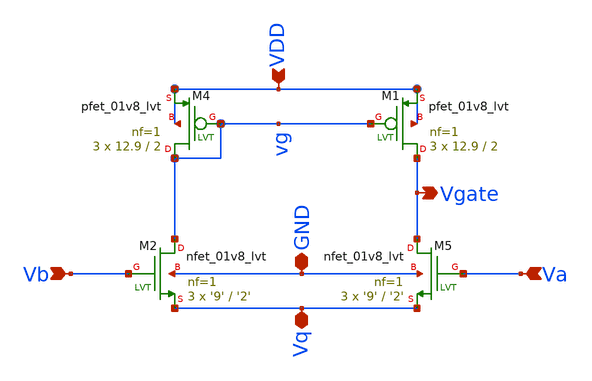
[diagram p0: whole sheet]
** sch_path: lvs/amplifier.sch
**.subckt amplifier VDD Vb Va Vq Vgate GND
*.ipin VDD
*.ipin Vb
*.ipin Va
*.iopin Vq
*.opin Vgate
*.iopin GND
XM5 Vgate Va Vq GND sky130_fd_pr__nfet_01v8_lvt L='2' W='9' nf=1 ad='int((nf+1)/2) * W/nf * 0.29' as='int((nf+2)/2) * W/nf * 0.29'
+ pd='2*int((nf+1)/2) * (W/nf + 0.29)' ps='2*int((nf+2)/2) * (W/nf + 0.29)' nrd='0.29 / W' nrs='0.29 / W'
+ sa=0 sb=0 sd=0 mult=3 m=3
XM2 vg Vb Vq GND sky130_fd_pr__nfet_01v8_lvt L='2' W='9' nf=1 ad='int((nf+1)/2) * W/nf * 0.29' as='int((nf+2)/2) * W/nf * 0.29'
+ pd='2*int((nf+1)/2) * (W/nf + 0.29)' ps='2*int((nf+2)/2) * (W/nf + 0.29)' nrd='0.29 / W' nrs='0.29 / W'
+ sa=0 sb=0 sd=0 mult=3 m=3
XM4 vg vg VDD VDD sky130_fd_pr__pfet_01v8_lvt L=2 W=12.9 nf=1 ad='int((nf+1)/2) * W/nf * 0.29' as='int((nf+2)/2) * W/nf * 0.29'
+ pd='2*int((nf+1)/2) * (W/nf + 0.29)' ps='2*int((nf+2)/2) * (W/nf + 0.29)' nrd='0.29 / W' nrs='0.29 / W'
+ sa=0 sb=0 sd=0 mult=3 m=3
XM1 Vgate vg VDD VDD sky130_fd_pr__pfet_01v8_lvt L=2 W=12.9 nf=1 ad='int((nf+1)/2) * W/nf * 0.29' as='int((nf+2)/2) * W/nf * 0.29'
+ pd='2*int((nf+1)/2) * (W/nf + 0.29)' ps='2*int((nf+2)/2) * (W/nf + 0.29)' nrd='0.29 / W' nrs='0.29 / W'
+ sa=0 sb=0 sd=0 mult=3 m=3
**.ends
.end
